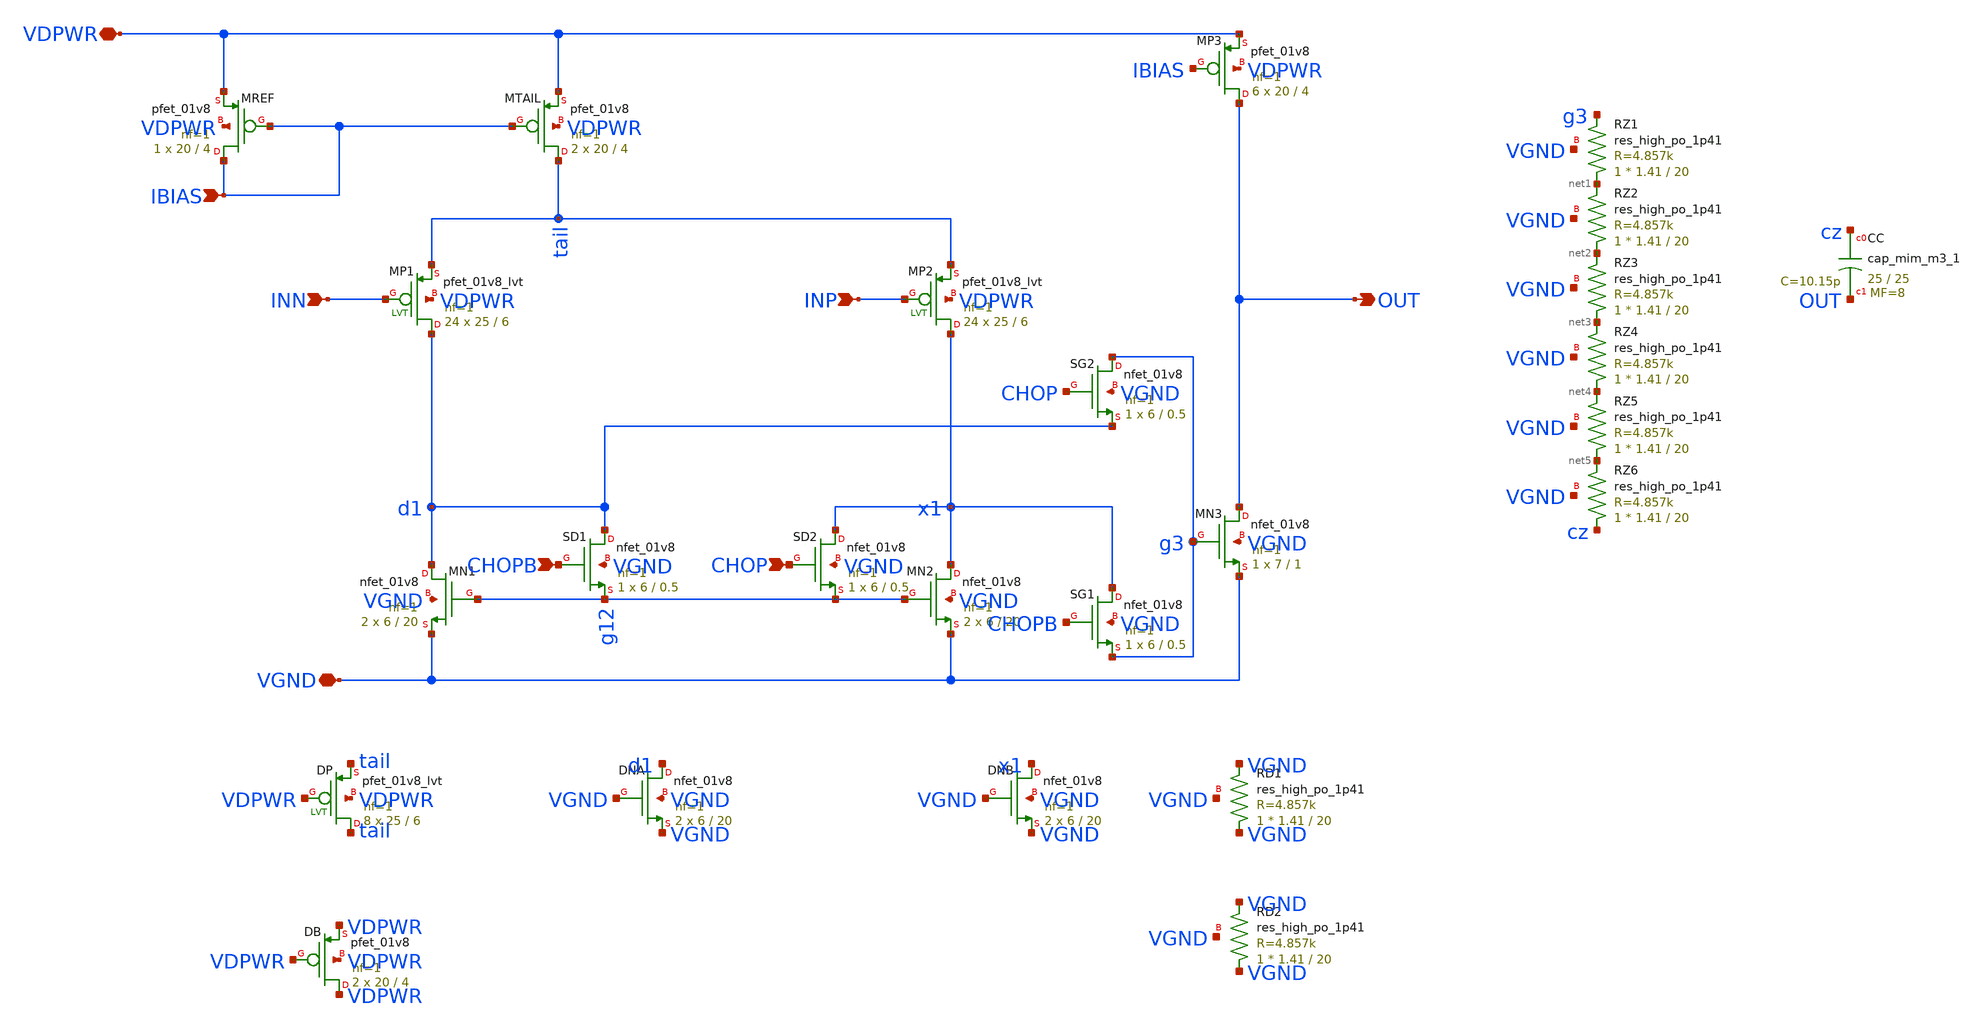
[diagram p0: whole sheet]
** sch_path: xschem/ota2s.sch
**.subckt ota2s INN INP IBIAS OUT VDPWR VGND CHOPB CHOP
*.ipin INN
*.ipin INP
*.ipin IBIAS
*.opin OUT
*.iopin VDPWR
*.iopin VGND
*.ipin CHOPB
*.ipin CHOP
XMREF IBIAS IBIAS VDPWR VDPWR sky130_fd_pr__pfet_01v8 L=4 W=20 nf=1 ad='int((1 + 1)/2) * 20 / 1 * 0.29'
+ as='int((1 + 2)/2) * 20 / 1 * 0.29' pd='2*int((1 + 1)/2) * (20 / 1 + 0.29)' ps='2*int((1 + 2)/2) * (20 / 1 + 0.29)'
+ nrd='0.29 / 20 ' nrs='0.29 / 20 ' sa=0 sb=0 sd=0 mult=1 m=1
XMTAIL tail IBIAS VDPWR VDPWR sky130_fd_pr__pfet_01v8 L=4 W=20 nf=1 ad='int((1 + 1)/2) * 20 / 1 * 0.29'
+ as='int((1 + 2)/2) * 20 / 1 * 0.29' pd='2*int((1 + 1)/2) * (20 / 1 + 0.29)' ps='2*int((1 + 2)/2) * (20 / 1 + 0.29)'
+ nrd='0.29 / 20 ' nrs='0.29 / 20 ' sa=0 sb=0 sd=0 mult=2 m=2
XMP1 d1 INN tail VDPWR sky130_fd_pr__pfet_01v8_lvt L=6 W=25 nf=1 ad='int((1 + 1)/2) * 25 / 1 * 0.29'
+ as='int((1 + 2)/2) * 25 / 1 * 0.29' pd='2*int((1 + 1)/2) * (25 / 1 + 0.29)' ps='2*int((1 + 2)/2) * (25 / 1 + 0.29)'
+ nrd='0.29 / 25 ' nrs='0.29 / 25 ' sa=0 sb=0 sd=0 mult=24 m=24
XMP2 x1 INP tail VDPWR sky130_fd_pr__pfet_01v8_lvt L=6 W=25 nf=1 ad='int((1 + 1)/2) * 25 / 1 * 0.29'
+ as='int((1 + 2)/2) * 25 / 1 * 0.29' pd='2*int((1 + 1)/2) * (25 / 1 + 0.29)' ps='2*int((1 + 2)/2) * (25 / 1 + 0.29)'
+ nrd='0.29 / 25 ' nrs='0.29 / 25 ' sa=0 sb=0 sd=0 mult=24 m=24
XMN1 d1 g12 VGND VGND sky130_fd_pr__nfet_01v8 L=20 W=6 nf=1 ad='int((1 + 1)/2) * 6 / 1 * 0.29' as='int((1 + 2)/2) * 6 / 1 * 0.29'
+ pd='2*int((1 + 1)/2) * (6 / 1 + 0.29)' ps='2*int((1 + 2)/2) * (6 / 1 + 0.29)' nrd='0.29 / 6 ' nrs='0.29 / 6 '
+ sa=0 sb=0 sd=0 mult=2 m=2
XMN2 x1 g12 VGND VGND sky130_fd_pr__nfet_01v8 L=20 W=6 nf=1 ad='int((1 + 1)/2) * 6 / 1 * 0.29' as='int((1 + 2)/2) * 6 / 1 * 0.29'
+ pd='2*int((1 + 1)/2) * (6 / 1 + 0.29)' ps='2*int((1 + 2)/2) * (6 / 1 + 0.29)' nrd='0.29 / 6 ' nrs='0.29 / 6 '
+ sa=0 sb=0 sd=0 mult=2 m=2
XMP3 OUT IBIAS VDPWR VDPWR sky130_fd_pr__pfet_01v8 L=4 W=20 nf=1 ad='int((1 + 1)/2) * 20 / 1 * 0.29'
+ as='int((1 + 2)/2) * 20 / 1 * 0.29' pd='2*int((1 + 1)/2) * (20 / 1 + 0.29)' ps='2*int((1 + 2)/2) * (20 / 1 + 0.29)'
+ nrd='0.29 / 20 ' nrs='0.29 / 20 ' sa=0 sb=0 sd=0 mult=6 m=6
XMN3 OUT g3 VGND VGND sky130_fd_pr__nfet_01v8 L=1 W=7 nf=1 ad='int((1 + 1)/2) * 7 / 1 * 0.29' as='int((1 + 2)/2) * 7 / 1 * 0.29'
+ pd='2*int((1 + 1)/2) * (7 / 1 + 0.29)' ps='2*int((1 + 2)/2) * (7 / 1 + 0.29)' nrd='0.29 / 7 ' nrs='0.29 / 7 '
+ sa=0 sb=0 sd=0 mult=1 m=1
XRZ1 net1 g3 VGND sky130_fd_pr__res_high_po_1p41 L=20 mult=1 m=1
XRZ2 net2 net1 VGND sky130_fd_pr__res_high_po_1p41 L=20 mult=1 m=1
XRZ3 net3 net2 VGND sky130_fd_pr__res_high_po_1p41 L=20 mult=1 m=1
XRZ4 net4 net3 VGND sky130_fd_pr__res_high_po_1p41 L=20 mult=1 m=1
XRZ5 net5 net4 VGND sky130_fd_pr__res_high_po_1p41 L=20 mult=1 m=1
XRZ6 cz net5 VGND sky130_fd_pr__res_high_po_1p41 L=20 mult=1 m=1
XCC cz OUT sky130_fd_pr__cap_mim_m3_1 W=25 L=25 MF=8 m=8
XDP tail VDPWR tail VDPWR sky130_fd_pr__pfet_01v8_lvt L=6 W=25 nf=1 ad='int((1 + 1)/2) * 25 / 1 * 0.29'
+ as='int((1 + 2)/2) * 25 / 1 * 0.29' pd='2*int((1 + 1)/2) * (25 / 1 + 0.29)' ps='2*int((1 + 2)/2) * (25 / 1 + 0.29)'
+ nrd='0.29 / 25 ' nrs='0.29 / 25 ' sa=0 sb=0 sd=0 mult=8 m=8
XDNA d1 VGND VGND VGND sky130_fd_pr__nfet_01v8 L=20 W=6 nf=1 ad='int((1 + 1)/2) * 6 / 1 * 0.29' as='int((1 + 2)/2) * 6 / 1 * 0.29'
+ pd='2*int((1 + 1)/2) * (6 / 1 + 0.29)' ps='2*int((1 + 2)/2) * (6 / 1 + 0.29)' nrd='0.29 / 6 ' nrs='0.29 / 6 '
+ sa=0 sb=0 sd=0 mult=2 m=2
XDNB x1 VGND VGND VGND sky130_fd_pr__nfet_01v8 L=20 W=6 nf=1 ad='int((1 + 1)/2) * 6 / 1 * 0.29' as='int((1 + 2)/2) * 6 / 1 * 0.29'
+ pd='2*int((1 + 1)/2) * (6 / 1 + 0.29)' ps='2*int((1 + 2)/2) * (6 / 1 + 0.29)' nrd='0.29 / 6 ' nrs='0.29 / 6 '
+ sa=0 sb=0 sd=0 mult=2 m=2
XDB VDPWR VDPWR VDPWR VDPWR sky130_fd_pr__pfet_01v8 L=4 W=20 nf=1 ad='int((1 + 1)/2) * 20 / 1 * 0.29'
+ as='int((1 + 2)/2) * 20 / 1 * 0.29' pd='2*int((1 + 1)/2) * (20 / 1 + 0.29)' ps='2*int((1 + 2)/2) * (20 / 1 + 0.29)'
+ nrd='0.29 / 20 ' nrs='0.29 / 20 ' sa=0 sb=0 sd=0 mult=2 m=2
XRD1 VGND VGND VGND sky130_fd_pr__res_high_po_1p41 L=20 mult=1 m=1
XRD2 VGND VGND VGND sky130_fd_pr__res_high_po_1p41 L=20 mult=1 m=1
XSD1 d1 CHOPB g12 VGND sky130_fd_pr__nfet_01v8 L=0.5 W=6 nf=1 ad='int((1 + 1)/2) * 6 / 1 * 0.29' as='int((1 + 2)/2) * 6 / 1 * 0.29'
+ pd='2*int((1 + 1)/2) * (6 / 1 + 0.29)' ps='2*int((1 + 2)/2) * (6 / 1 + 0.29)' nrd='0.29 / 6 ' nrs='0.29 / 6 '
+ sa=0 sb=0 sd=0 mult=1 m=1
XSD2 x1 CHOP g12 VGND sky130_fd_pr__nfet_01v8 L=0.5 W=6 nf=1 ad='int((1 + 1)/2) * 6 / 1 * 0.29' as='int((1 + 2)/2) * 6 / 1 * 0.29'
+ pd='2*int((1 + 1)/2) * (6 / 1 + 0.29)' ps='2*int((1 + 2)/2) * (6 / 1 + 0.29)' nrd='0.29 / 6 ' nrs='0.29 / 6 '
+ sa=0 sb=0 sd=0 mult=1 m=1
XSG2 g3 CHOP d1 VGND sky130_fd_pr__nfet_01v8 L=0.5 W=6 nf=1 ad='int((1 + 1)/2) * 6 / 1 * 0.29' as='int((1 + 2)/2) * 6 / 1 * 0.29'
+ pd='2*int((1 + 1)/2) * (6 / 1 + 0.29)' ps='2*int((1 + 2)/2) * (6 / 1 + 0.29)' nrd='0.29 / 6 ' nrs='0.29 / 6 '
+ sa=0 sb=0 sd=0 mult=1 m=1
XSG1 x1 CHOPB g3 VGND sky130_fd_pr__nfet_01v8 L=0.5 W=6 nf=1 ad='int((1 + 1)/2) * 6 / 1 * 0.29' as='int((1 + 2)/2) * 6 / 1 * 0.29'
+ pd='2*int((1 + 1)/2) * (6 / 1 + 0.29)' ps='2*int((1 + 2)/2) * (6 / 1 + 0.29)' nrd='0.29 / 6 ' nrs='0.29 / 6 '
+ sa=0 sb=0 sd=0 mult=1 m=1
**.ends
.end
